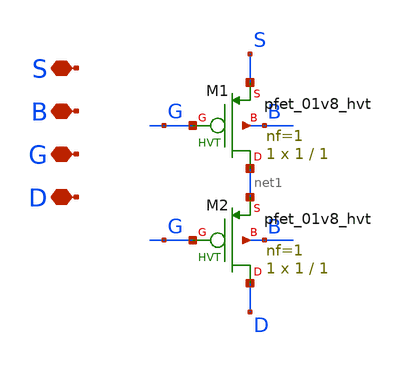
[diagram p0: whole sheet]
** sch_path: INA_layout_v2/bias/pfet_2series.sch
**.subckt pfet_2series S B G D
*.iopin S
*.iopin B
*.iopin G
*.iopin D
XM1 net1 G S B sky130_fd_pr__pfet_01v8_hvt L=1 W=1 nf=1 ad='int((nf+1)/2) * W/nf * 0.29' as='int((nf+2)/2) * W/nf * 0.29'
+ pd='2*int((nf+1)/2) * (W/nf + 0.29)' ps='2*int((nf+2)/2) * (W/nf + 0.29)' nrd='0.29 / W' nrs='0.29 / W'
+ sa=0 sb=0 sd=0 mult=1 m=1
XM2 D G net1 B sky130_fd_pr__pfet_01v8_hvt L=1 W=1 nf=1 ad='int((nf+1)/2) * W/nf * 0.29' as='int((nf+2)/2) * W/nf * 0.29'
+ pd='2*int((nf+1)/2) * (W/nf + 0.29)' ps='2*int((nf+2)/2) * (W/nf + 0.29)' nrd='0.29 / W' nrs='0.29 / W'
+ sa=0 sb=0 sd=0 mult=1 m=1
**.ends
.end
